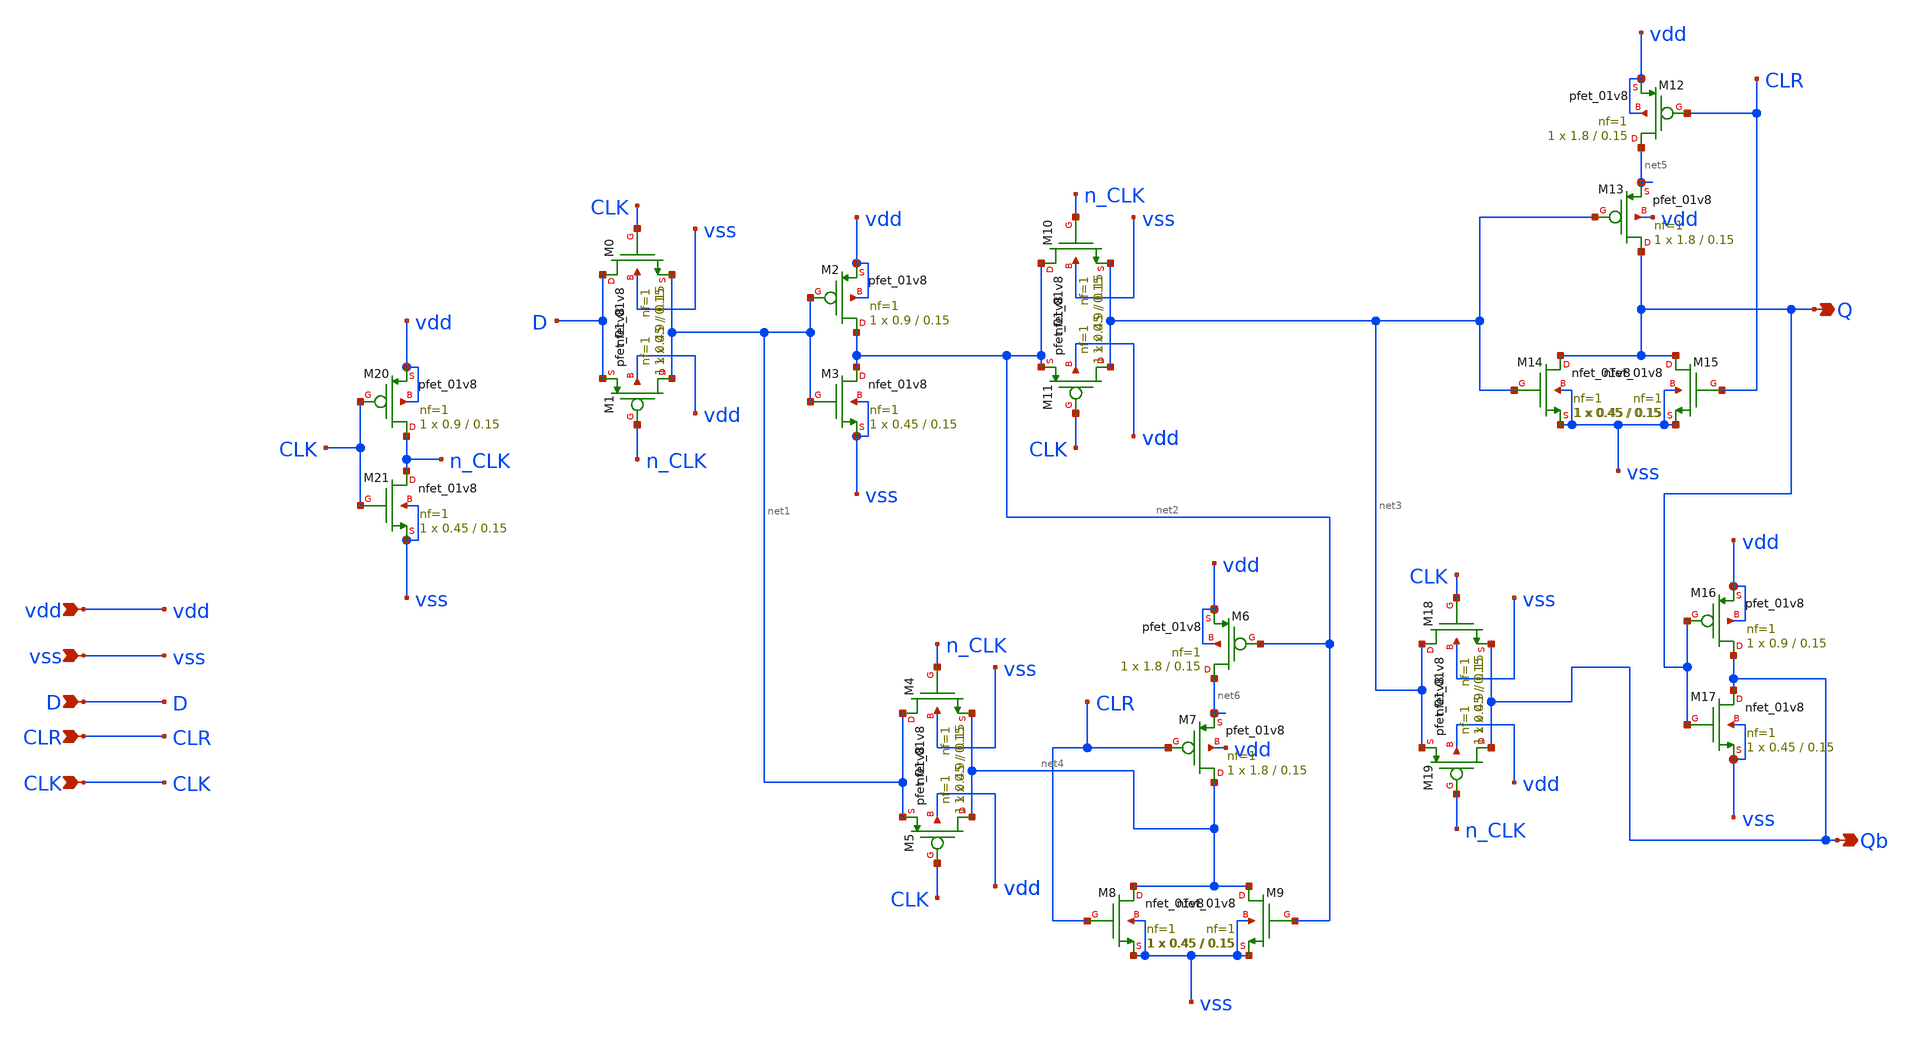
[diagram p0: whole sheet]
** sch_path: track_vlsi/somoza/sch/dffc.sch
**.subckt dffc vdd vss D CLR CLK Q Qb
*.ipin vdd
*.ipin vss
*.ipin D
*.ipin CLR
*.ipin CLK
*.opin Q
*.opin Qb
XM21 n_CLK CLK vss vss sky130_fd_pr__nfet_01v8 L=0.15 W=0.45 nf=1 ad='int((nf+1)/2) * W/nf * 0.29' as='int((nf+2)/2) * W/nf * 0.29'
+ pd='2*int((nf+1)/2) * (W/nf + 0.29)' ps='2*int((nf+2)/2) * (W/nf + 0.29)' nrd='0.29 / W' nrs='0.29 / W'
+ sa=0 sb=0 sd=0 mult=1 m=1
XM20 n_CLK CLK vdd vdd sky130_fd_pr__pfet_01v8 L=0.15 W=0.9 nf=1 ad='int((nf+1)/2) * W/nf * 0.29' as='int((nf+2)/2) * W/nf * 0.29'
+ pd='2*int((nf+1)/2) * (W/nf + 0.29)' ps='2*int((nf+2)/2) * (W/nf + 0.29)' nrd='0.29 / W' nrs='0.29 / W'
+ sa=0 sb=0 sd=0 mult=1 m=1
XM1 net1 n_CLK D vdd sky130_fd_pr__pfet_01v8 L=0.15 W=0.9 nf=1 ad='int((nf+1)/2) * W/nf * 0.29' as='int((nf+2)/2) * W/nf * 0.29'
+ pd='2*int((nf+1)/2) * (W/nf + 0.29)' ps='2*int((nf+2)/2) * (W/nf + 0.29)' nrd='0.29 / W' nrs='0.29 / W'
+ sa=0 sb=0 sd=0 mult=1 m=1
XM0 D CLK net1 vss sky130_fd_pr__nfet_01v8 L=0.15 W=0.45 nf=1 ad='int((nf+1)/2) * W/nf * 0.29' as='int((nf+2)/2) * W/nf * 0.29'
+ pd='2*int((nf+1)/2) * (W/nf + 0.29)' ps='2*int((nf+2)/2) * (W/nf + 0.29)' nrd='0.29 / W' nrs='0.29 / W'
+ sa=0 sb=0 sd=0 mult=1 m=1
XM3 net2 net1 vss vss sky130_fd_pr__nfet_01v8 L=0.15 W=0.45 nf=1 ad='int((nf+1)/2) * W/nf * 0.29' as='int((nf+2)/2) * W/nf * 0.29'
+ pd='2*int((nf+1)/2) * (W/nf + 0.29)' ps='2*int((nf+2)/2) * (W/nf + 0.29)' nrd='0.29 / W' nrs='0.29 / W'
+ sa=0 sb=0 sd=0 mult=1 m=1
XM2 net2 net1 vdd vdd sky130_fd_pr__pfet_01v8 L=0.15 W=0.9 nf=1 ad='int((nf+1)/2) * W/nf * 0.29' as='int((nf+2)/2) * W/nf * 0.29'
+ pd='2*int((nf+1)/2) * (W/nf + 0.29)' ps='2*int((nf+2)/2) * (W/nf + 0.29)' nrd='0.29 / W' nrs='0.29 / W'
+ sa=0 sb=0 sd=0 mult=1 m=1
XM11 net3 CLK net2 vdd sky130_fd_pr__pfet_01v8 L=0.15 W=0.9 nf=1 ad='int((nf+1)/2) * W/nf * 0.29' as='int((nf+2)/2) * W/nf * 0.29'
+ pd='2*int((nf+1)/2) * (W/nf + 0.29)' ps='2*int((nf+2)/2) * (W/nf + 0.29)' nrd='0.29 / W' nrs='0.29 / W'
+ sa=0 sb=0 sd=0 mult=1 m=1
XM10 net2 n_CLK net3 vss sky130_fd_pr__nfet_01v8 L=0.15 W=0.45 nf=1 ad='int((nf+1)/2) * W/nf * 0.29'
+ as='int((nf+2)/2) * W/nf * 0.29' pd='2*int((nf+1)/2) * (W/nf + 0.29)' ps='2*int((nf+2)/2) * (W/nf + 0.29)'
+ nrd='0.29 / W' nrs='0.29 / W' sa=0 sb=0 sd=0 mult=1 m=1
XM5 net4 CLK net1 vdd sky130_fd_pr__pfet_01v8 L=0.15 W=0.9 nf=1 ad='int((nf+1)/2) * W/nf * 0.29' as='int((nf+2)/2) * W/nf * 0.29'
+ pd='2*int((nf+1)/2) * (W/nf + 0.29)' ps='2*int((nf+2)/2) * (W/nf + 0.29)' nrd='0.29 / W' nrs='0.29 / W'
+ sa=0 sb=0 sd=0 mult=1 m=1
XM4 net1 n_CLK net4 vss sky130_fd_pr__nfet_01v8 L=0.15 W=0.45 nf=1 ad='int((nf+1)/2) * W/nf * 0.29' as='int((nf+2)/2) * W/nf * 0.29'
+ pd='2*int((nf+1)/2) * (W/nf + 0.29)' ps='2*int((nf+2)/2) * (W/nf + 0.29)' nrd='0.29 / W' nrs='0.29 / W'
+ sa=0 sb=0 sd=0 mult=1 m=1
XM13 Q net3 net5 vdd sky130_fd_pr__pfet_01v8 L=0.15 W=1.8 nf=1 ad='int((nf+1)/2) * W/nf * 0.29' as='int((nf+2)/2) * W/nf * 0.29'
+ pd='2*int((nf+1)/2) * (W/nf + 0.29)' ps='2*int((nf+2)/2) * (W/nf + 0.29)' nrd='0.29 / W' nrs='0.29 / W'
+ sa=0 sb=0 sd=0 mult=1 m=1
XM12 net5 CLR vdd vdd sky130_fd_pr__pfet_01v8 L=0.15 W=1.8 nf=1 ad='int((nf+1)/2) * W/nf * 0.29' as='int((nf+2)/2) * W/nf * 0.29'
+ pd='2*int((nf+1)/2) * (W/nf + 0.29)' ps='2*int((nf+2)/2) * (W/nf + 0.29)' nrd='0.29 / W' nrs='0.29 / W'
+ sa=0 sb=0 sd=0 mult=1 m=1
XM8 net4 CLR vss vss sky130_fd_pr__nfet_01v8 L=0.15 W=0.45 nf=1 ad='int((nf+1)/2) * W/nf * 0.29' as='int((nf+2)/2) * W/nf * 0.29'
+ pd='2*int((nf+1)/2) * (W/nf + 0.29)' ps='2*int((nf+2)/2) * (W/nf + 0.29)' nrd='0.29 / W' nrs='0.29 / W'
+ sa=0 sb=0 sd=0 mult=1 m=1
XM7 net4 CLR net6 vdd sky130_fd_pr__pfet_01v8 L=0.15 W=1.8 nf=1 ad='int((nf+1)/2) * W/nf * 0.29' as='int((nf+2)/2) * W/nf * 0.29'
+ pd='2*int((nf+1)/2) * (W/nf + 0.29)' ps='2*int((nf+2)/2) * (W/nf + 0.29)' nrd='0.29 / W' nrs='0.29 / W'
+ sa=0 sb=0 sd=0 mult=1 m=1
XM6 net6 net2 vdd vdd sky130_fd_pr__pfet_01v8 L=0.15 W=1.8 nf=1 ad='int((nf+1)/2) * W/nf * 0.29' as='int((nf+2)/2) * W/nf * 0.29'
+ pd='2*int((nf+1)/2) * (W/nf + 0.29)' ps='2*int((nf+2)/2) * (W/nf + 0.29)' nrd='0.29 / W' nrs='0.29 / W'
+ sa=0 sb=0 sd=0 mult=1 m=1
XM9 net4 net2 vss vss sky130_fd_pr__nfet_01v8 L=0.15 W=0.45 nf=1 ad='int((nf+1)/2) * W/nf * 0.29' as='int((nf+2)/2) * W/nf * 0.29'
+ pd='2*int((nf+1)/2) * (W/nf + 0.29)' ps='2*int((nf+2)/2) * (W/nf + 0.29)' nrd='0.29 / W' nrs='0.29 / W'
+ sa=0 sb=0 sd=0 mult=1 m=1
XM14 Q net3 vss vss sky130_fd_pr__nfet_01v8 L=0.15 W=0.45 nf=1 ad='int((nf+1)/2) * W/nf * 0.29' as='int((nf+2)/2) * W/nf * 0.29'
+ pd='2*int((nf+1)/2) * (W/nf + 0.29)' ps='2*int((nf+2)/2) * (W/nf + 0.29)' nrd='0.29 / W' nrs='0.29 / W'
+ sa=0 sb=0 sd=0 mult=1 m=1
XM15 Q CLR vss vss sky130_fd_pr__nfet_01v8 L=0.15 W=0.45 nf=1 ad='int((nf+1)/2) * W/nf * 0.29' as='int((nf+2)/2) * W/nf * 0.29'
+ pd='2*int((nf+1)/2) * (W/nf + 0.29)' ps='2*int((nf+2)/2) * (W/nf + 0.29)' nrd='0.29 / W' nrs='0.29 / W'
+ sa=0 sb=0 sd=0 mult=1 m=1
XM19 Qb n_CLK net3 vdd sky130_fd_pr__pfet_01v8 L=0.15 W=0.9 nf=1 ad='int((nf+1)/2) * W/nf * 0.29' as='int((nf+2)/2) * W/nf * 0.29'
+ pd='2*int((nf+1)/2) * (W/nf + 0.29)' ps='2*int((nf+2)/2) * (W/nf + 0.29)' nrd='0.29 / W' nrs='0.29 / W'
+ sa=0 sb=0 sd=0 mult=1 m=1
XM18 net3 CLK Qb vss sky130_fd_pr__nfet_01v8 L=0.15 W=0.45 nf=1 ad='int((nf+1)/2) * W/nf * 0.29' as='int((nf+2)/2) * W/nf * 0.29'
+ pd='2*int((nf+1)/2) * (W/nf + 0.29)' ps='2*int((nf+2)/2) * (W/nf + 0.29)' nrd='0.29 / W' nrs='0.29 / W'
+ sa=0 sb=0 sd=0 mult=1 m=1
XM17 Qb Q vss vss sky130_fd_pr__nfet_01v8 L=0.15 W=0.45 nf=1 ad='int((nf+1)/2) * W/nf * 0.29' as='int((nf+2)/2) * W/nf * 0.29'
+ pd='2*int((nf+1)/2) * (W/nf + 0.29)' ps='2*int((nf+2)/2) * (W/nf + 0.29)' nrd='0.29 / W' nrs='0.29 / W'
+ sa=0 sb=0 sd=0 mult=1 m=1
XM16 Qb Q vdd vdd sky130_fd_pr__pfet_01v8 L=0.15 W=0.9 nf=1 ad='int((nf+1)/2) * W/nf * 0.29' as='int((nf+2)/2) * W/nf * 0.29'
+ pd='2*int((nf+1)/2) * (W/nf + 0.29)' ps='2*int((nf+2)/2) * (W/nf + 0.29)' nrd='0.29 / W' nrs='0.29 / W'
+ sa=0 sb=0 sd=0 mult=1 m=1
**.ends
.end
